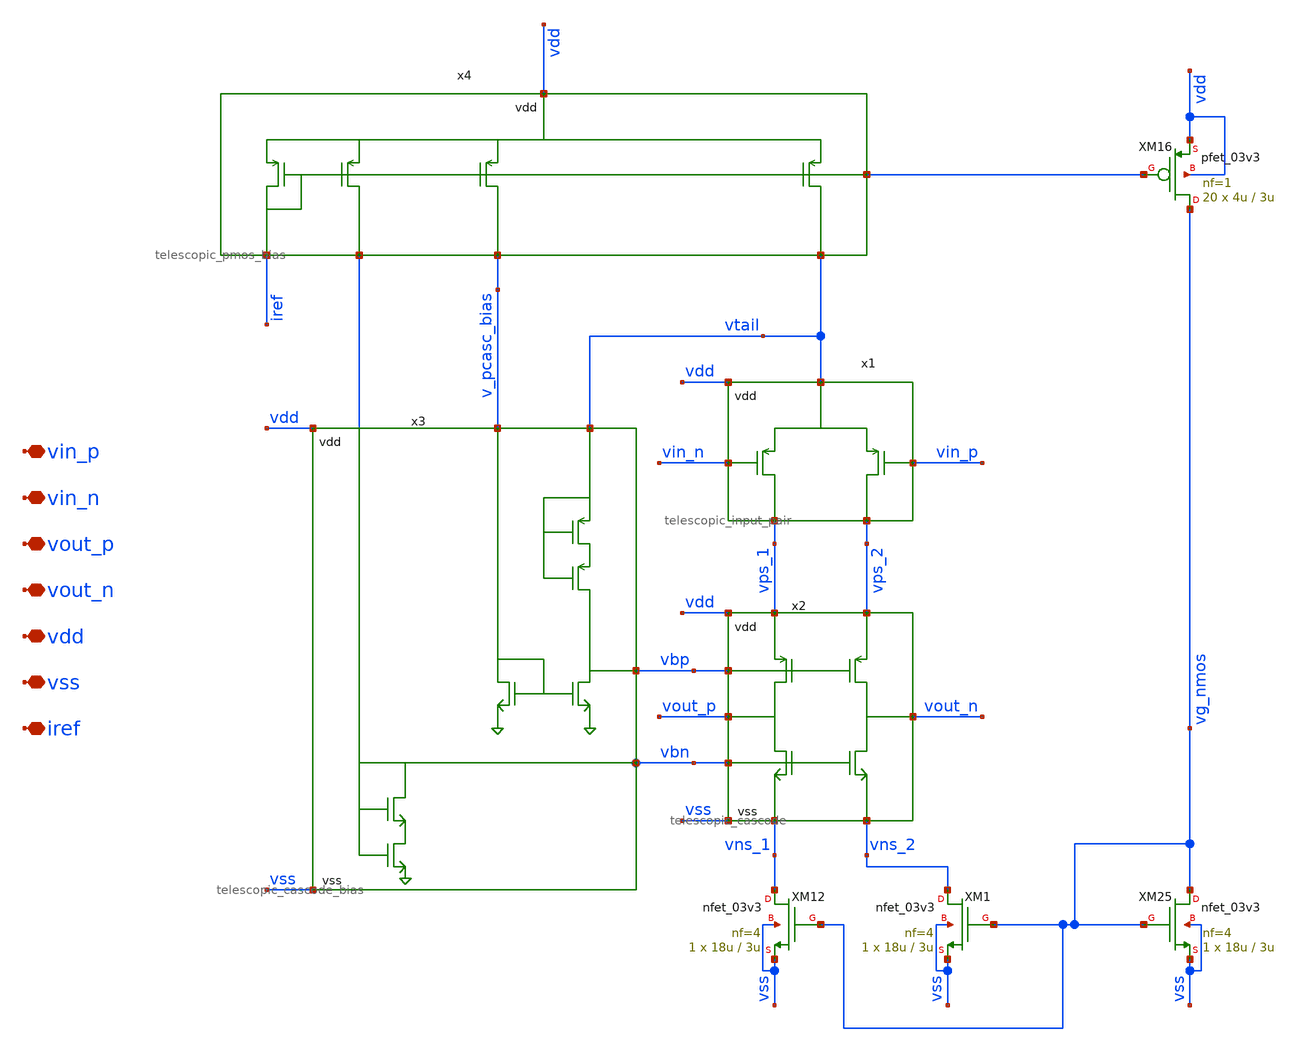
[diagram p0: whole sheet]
** sch_path: xschem/archive/rrl/telescopic_no_cmfb.sch
**.subckt telescopic_no_cmfb vin_p vin_n vout_p vout_n vdd vss iref
*.iopin vin_p
*.iopin vin_n
*.iopin vout_p
*.iopin vout_n
*.iopin vdd
*.iopin vss
*.iopin iref
x1 vtail vdd vin_n vin_p vps_1 vps_2 telescopic_input_pair
x2 vdd vss vps_1 vps_2 vns_1 vns_2 vout_p vout_n vbp vbn telescopic_cascode
x3 vbn v_pcasc_bias vtail vbp vss vdd telescopic_cascode_bias
x4 vdd vbn v_pcasc_bias vtail iref telescopic_pmos_bias
XM16 vg_nmos iref vdd vdd pfet_03v3 L=3u W=4u nf=1 ad='int((nf+1)/2) * W/nf * 0.18u' as='int((nf+2)/2) * W/nf * 0.18u'
+ pd='2*int((nf+1)/2) * (W/nf + 0.18u)' ps='2*int((nf+2)/2) * (W/nf + 0.18u)' nrd='0.18u / W' nrs='0.18u / W'
+ sa=0 sb=0 sd=0 m=20
XM12 vns_1 vg_nmos vss vss nfet_03v3 L=3u W=18u nf=4 ad='int((nf+1)/2) * W/nf * 0.18u' as='int((nf+2)/2) * W/nf * 0.18u'
+ pd='2*int((nf+1)/2) * (W/nf + 0.18u)' ps='2*int((nf+2)/2) * (W/nf + 0.18u)' nrd='0.18u / W' nrs='0.18u / W'
+ sa=0 sb=0 sd=0 m=1
XM25 vg_nmos vg_nmos vss vss nfet_03v3 L=3u W=18u nf=4 ad='int((nf+1)/2) * W/nf * 0.18u' as='int((nf+2)/2) * W/nf * 0.18u'
+ pd='2*int((nf+1)/2) * (W/nf + 0.18u)' ps='2*int((nf+2)/2) * (W/nf + 0.18u)' nrd='0.18u / W' nrs='0.18u / W'
+ sa=0 sb=0 sd=0 m=1
XM1 vns_2 vg_nmos vss vss nfet_03v3 L=3u W=18u nf=4 ad='int((nf+1)/2) * W/nf * 0.18u' as='int((nf+2)/2) * W/nf * 0.18u'
+ pd='2*int((nf+1)/2) * (W/nf + 0.18u)' ps='2*int((nf+2)/2) * (W/nf + 0.18u)' nrd='0.18u / W' nrs='0.18u / W'
+ sa=0 sb=0 sd=0 m=1
**.ends
.end
